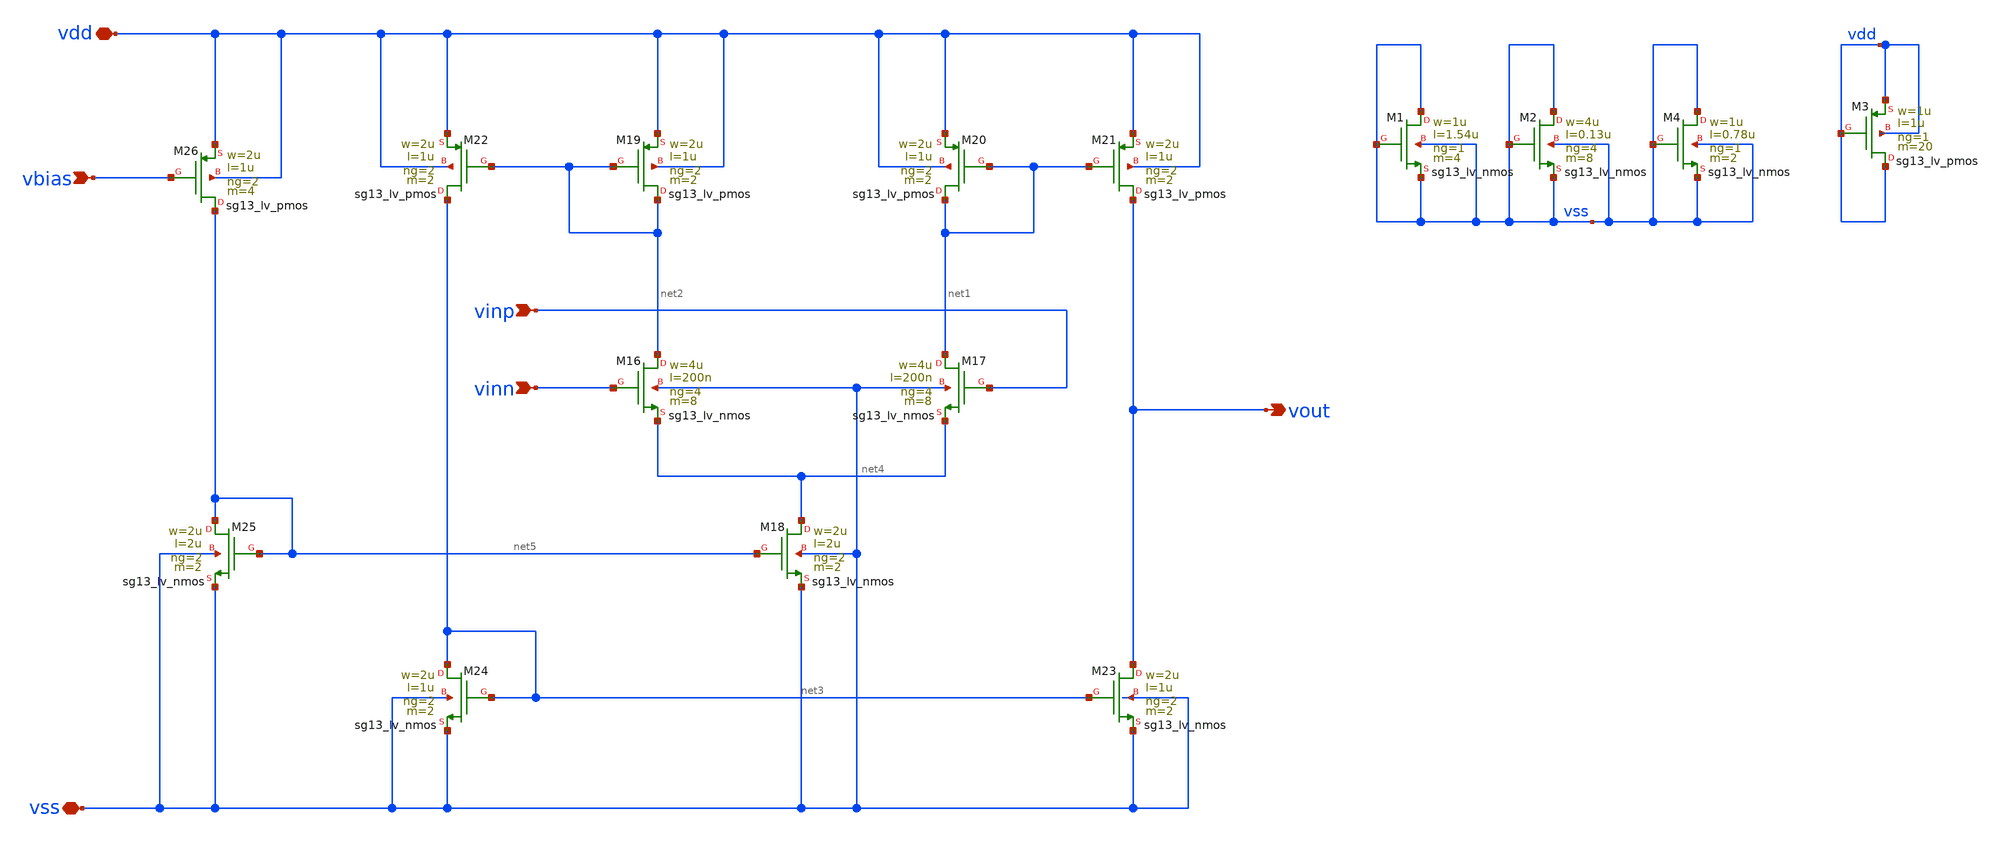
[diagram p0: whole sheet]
** sch_path: v2_feature_extr_withf/a_buffN.sch
* (c) 2026 Arianna Rubino, Apache-2.0 license
**.subckt a_buffN vinp vinn vbias vout vdd vss
*.ipin vinp
*.ipin vinn
*.ipin vbias
*.opin vout
*.iopin vdd
*.iopin vss
XM16 net2 vinn net4 vss sg13_lv_nmos w=4u l=200n ng=4 m=8 mm_ok=1
XM17 net1 vinp net4 vss sg13_lv_nmos w=4u l=200n ng=4 m=8 mm_ok=1
XM18 net4 net5 vss vss sg13_lv_nmos w=2u l=2u ng=2 m=2 mm_ok=1
XM19 net2 net2 vdd vdd sg13_lv_pmos w=2u l=1u ng=2 m=2 mm_ok=1
XM20 net1 net1 vdd vdd sg13_lv_pmos w=2u l=1u ng=2 m=2 mm_ok=1
XM21 vout net1 vdd vdd sg13_lv_pmos w=2u l=1u ng=2 m=2 mm_ok=1
XM22 net3 net2 vdd vdd sg13_lv_pmos w=2u l=1u ng=2 m=2 mm_ok=1
XM23 vout net3 vss vss sg13_lv_nmos w=2u l=1u ng=2 m=2 mm_ok=1
XM24 net3 net3 vss vss sg13_lv_nmos w=2u l=1u ng=2 m=2 mm_ok=1
XM25 net5 net5 vss vss sg13_lv_nmos w=2u l=2u ng=2 m=2 mm_ok=1
XM26 net5 vbias vdd vdd sg13_lv_pmos w=2u l=1u ng=2 m=4 mm_ok=1
XM1 vss vss vss vss sg13_lv_nmos w=1u l=1.54u ng=1 m=4 mm_ok=1
XM2 vss vss vss vss sg13_lv_nmos w=4u l=0.13u ng=4 m=8 mm_ok=1
XM3 vdd vdd vdd vdd sg13_lv_pmos w=1u l=1u ng=1 m=20 mm_ok=1
XM4 vss vss vss vss sg13_lv_nmos w=1u l=0.78u ng=1 m=2 mm_ok=1
**.ends
.end
